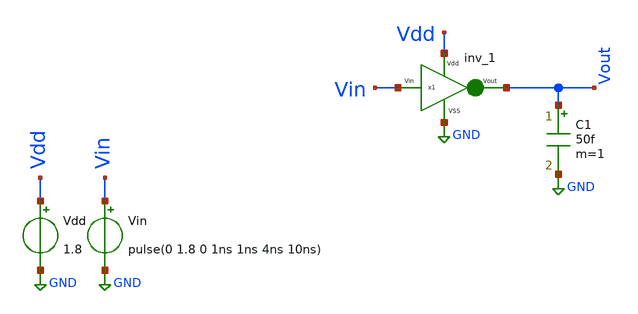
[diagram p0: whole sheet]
** sch_path: xschem files/inv_dc.sch
**.subckt inv_dc
Vin Vin GND pulse(0 1.8 0 1ns 1ns 4ns 10ns)
Vdd Vdd GND 1.8
C1 Vout GND 50f m=1
x1 Vdd Vout Vin GND inv_1
**** begin user architecture code


.lib /usr/local/share/pdk/sky130A/libs.tech/ngspice/sky130.lib.spice tt
* .include /home/harshit/.xschem/inv.spice
.tran 100ps 20ns
.dc Vin 0 1.8 1m
.save all
* .let curr = @m.x1.xm1.msky130_fd_pr__nfet_01v8[id]
.save i(c1)
* .func foo(v(vout)) {abs(deriv(v(vout))) >= 1}
.options savecurrents
.end

**** end user architecture code
**.ends

* expanding   symbol:  /home/harshit/.xschem/inv_1.sym # of pins=4
** sym_path: xschem files/inv_1.sym
** sch_path: xschem files/inv_1.sch
.subckt inv_1 Vdd Vout Vin VSS
*.ipin Vdd
*.ipin VSS
*.opin Vout
*.ipin Vin
XM1 Vout Vin VSS VSS sky130_fd_pr__nfet_01v8 L=0.15 W=1.05 nf=1 ad='int((nf+1)/2) * W/nf * 0.29' as='int((nf+2)/2) * W/nf * 0.29'
+ pd='2*int((nf+1)/2) * (W/nf + 0.29)' ps='2*int((nf+2)/2) * (W/nf + 0.29)' nrd='0.29 / W' nrs='0.29 / W'
+ sa=0 sb=0 sd=0 mult=1 m=1
XM2 Vout Vin Vdd Vdd sky130_fd_pr__pfet_01v8 L=0.15 W=2.1 nf=1 ad='int((nf+1)/2) * W/nf * 0.29' as='int((nf+2)/2) * W/nf * 0.29'
+ pd='2*int((nf+1)/2) * (W/nf + 0.29)' ps='2*int((nf+2)/2) * (W/nf + 0.29)' nrd='0.29 / W' nrs='0.29 / W'
+ sa=0 sb=0 sd=0 mult=1 m=1
.ends

.GLOBAL GND
.end
